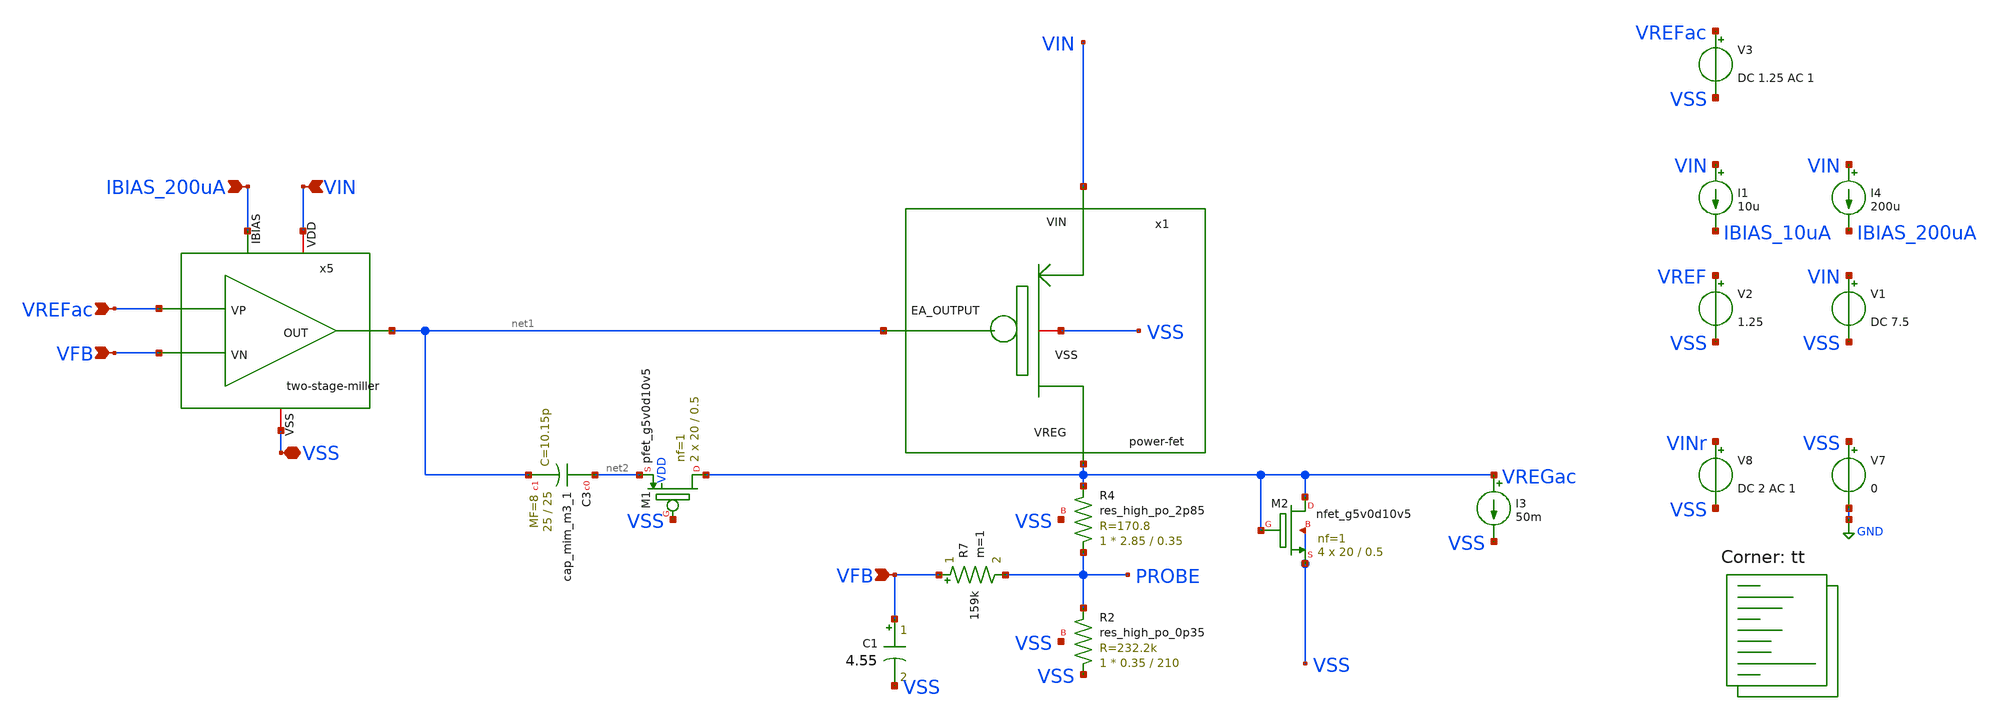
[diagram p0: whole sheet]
** sch_path: xschem/ldo-core/loop-gain.sch
**.subckt loop-gain VFB VREFac IBIAS_200uA VIN VSS VFB
*.ipin VFB
*.ipin VREFac
*.ipin IBIAS_200uA
*.ipin VIN
*.iopin VSS
*.ipin VFB
V2 VREF VSS 1.25
V7 VSS GND 0
V8 VINr VSS DC 2 AC 1
I4 VIN IBIAS_200uA 200u
I1 VIN IBIAS_10uA 10u
x1 VIN VSS net1 VREGac power-fet
XR4 PROBE VREGac VSS sky130_fd_pr__res_high_po_2p85 L=0.35 mult=1 m=1
x5 VIN net1 VREFac VFB IBIAS_200uA VSS two-stage-miller
I3 VREGac VSS 50m
V1 VIN VSS DC 7.5
XR2 VSS PROBE VSS sky130_fd_pr__res_high_po_0p35 L=210 mult=1 m=1
R7 VFB PROBE 159k m=1
C1 VFB VSS 4.55 m=1
V3 VREFac VSS DC 1.25 AC 1
XC3 net2 net1 sky130_fd_pr__cap_mim_m3_1 W=25 L=25 MF=8 m=8
XM2 VREGac VREGac VSS VSS sky130_fd_pr__nfet_g5v0d10v5 L=0.5 W=20 nf=1 ad='int((nf+1)/2) * W/nf * 0.29'
+ as='int((nf+2)/2) * W/nf * 0.29' pd='2*int((nf+1)/2) * (W/nf + 0.29)' ps='2*int((nf+2)/2) * (W/nf + 0.29)'
+ nrd='0.29 / W' nrs='0.29 / W' sa=0 sb=0 sd=0 mult=4 m=4
XM1 VREGac VSS net2 VDD sky130_fd_pr__pfet_g5v0d10v5 L=0.5 W=20 nf=1 ad='int((nf+1)/2) * W/nf * 0.29'
+ as='int((nf+2)/2) * W/nf * 0.29' pd='2*int((nf+1)/2) * (W/nf + 0.29)' ps='2*int((nf+2)/2) * (W/nf + 0.29)'
+ nrd='0.29 / W' nrs='0.29 / W' sa=0 sb=0 sd=0 mult=2 m=2
**** begin user architecture code



.temp 27
.control

AC DEC 100 1 100G
let PSRR = -20*log10(VREG)
* Phase (same expression form you used — adopted)
let phase = 180 + 180*cph( v(PROBE) )/pi

* 1. Calculate the True Loop Gain (T)
  * T = V_return / V_injected
  let loop_gain_complex = v(PROBE)
  let lg_db = db(loop_gain_complex)
  let lg_ph = ph(loop_gain_complex) * 180 / PI

* 2. Normalize Phase (so it starts at 0 or 180 depending on your EA polarity)
  * For a standard LDO, we want to see how far we are from -180 degrees.
  let phase_margin_plot = lg_ph + 180

* 3. Automatically find the Phase Margin value
  meas ac f_unity when lg_db=0
  meas ac PM_value find phase_margin_plot when frequency=f_unity

  echo Unity Gain Frequency: $&f_unity Hz
  echo Phase Margin: $&PM_value degrees

  plot lg_db
  plot lg_db phase_margin_plot


	plot PSRR
	plot phase

.endc


.lib $::SKYWATER_MODELS/sky130.lib.spice tt
**** end user architecture code
**.ends
.GLOBAL GND
.end
